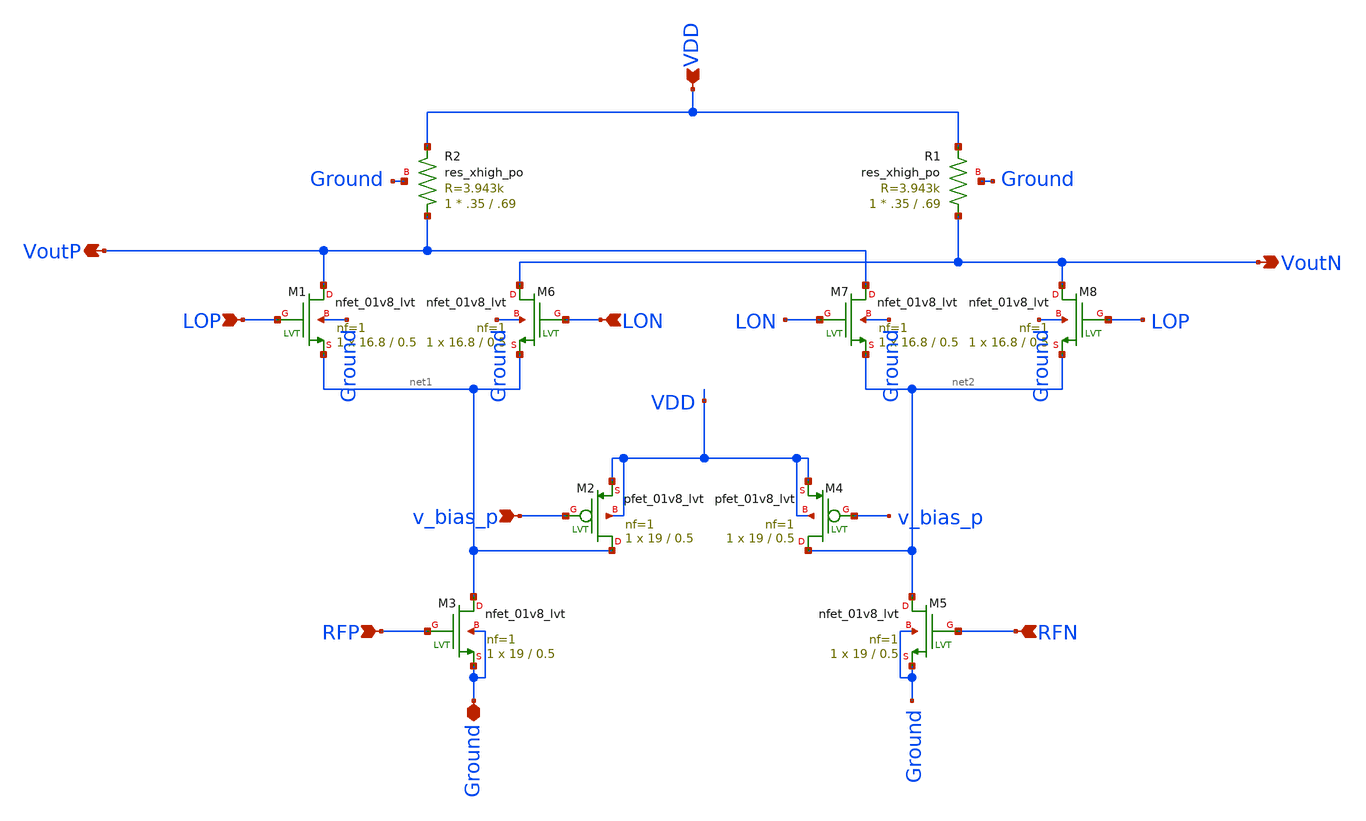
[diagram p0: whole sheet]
** sch_path: skywater_stuff/ECE631_RF_CMOS/Mixer_LVS_test1.sch
**.subckt Mixer_LVS_test1 v_bias_p RFP RFN LOP LON VoutP VoutN Ground VDD
*.ipin v_bias_p
*.ipin RFP
*.ipin RFN
*.ipin LOP
*.ipin LON
*.opin VoutP
*.opin VoutN
*.iopin Ground
*.ipin VDD
XM1 VoutP LOP net1 Ground sky130_fd_pr__nfet_01v8_lvt L=0.5 W=16.8 nf=1 ad='int((nf+1)/2) * W/nf * 0.29'
+ as='int((nf+2)/2) * W/nf * 0.29' pd='2*int((nf+1)/2) * (W/nf + 0.29)' ps='2*int((nf+2)/2) * (W/nf + 0.29)'
+ nrd='0.29 / W' nrs='0.29 / W' sa=0 sb=0 sd=0 mult=1 m=1
XM2 net1 v_bias_p VDD VDD sky130_fd_pr__pfet_01v8_lvt L=0.5 W=19 nf=1 ad='int((nf+1)/2) * W/nf * 0.29'
+ as='int((nf+2)/2) * W/nf * 0.29' pd='2*int((nf+1)/2) * (W/nf + 0.29)' ps='2*int((nf+2)/2) * (W/nf + 0.29)'
+ nrd='0.29 / W' nrs='0.29 / W' sa=0 sb=0 sd=0 mult=1 m=1
XM6 VoutN LON net1 Ground sky130_fd_pr__nfet_01v8_lvt L=0.5 W=16.8 nf=1 ad='int((nf+1)/2) * W/nf * 0.29'
+ as='int((nf+2)/2) * W/nf * 0.29' pd='2*int((nf+1)/2) * (W/nf + 0.29)' ps='2*int((nf+2)/2) * (W/nf + 0.29)'
+ nrd='0.29 / W' nrs='0.29 / W' sa=0 sb=0 sd=0 mult=1 m=1
XM7 VoutP LON net2 Ground sky130_fd_pr__nfet_01v8_lvt L=0.5 W=16.8 nf=1 ad='int((nf+1)/2) * W/nf * 0.29'
+ as='int((nf+2)/2) * W/nf * 0.29' pd='2*int((nf+1)/2) * (W/nf + 0.29)' ps='2*int((nf+2)/2) * (W/nf + 0.29)'
+ nrd='0.29 / W' nrs='0.29 / W' sa=0 sb=0 sd=0 mult=1 m=1
XM8 VoutN LOP net2 Ground sky130_fd_pr__nfet_01v8_lvt L=0.5 W=16.8 nf=1 ad='int((nf+1)/2) * W/nf * 0.29'
+ as='int((nf+2)/2) * W/nf * 0.29' pd='2*int((nf+1)/2) * (W/nf + 0.29)' ps='2*int((nf+2)/2) * (W/nf + 0.29)'
+ nrd='0.29 / W' nrs='0.29 / W' sa=0 sb=0 sd=0 mult=1 m=1
XM3 net1 RFP Ground Ground sky130_fd_pr__nfet_01v8_lvt L=0.5 W=19 nf=1 ad='int((nf+1)/2) * W/nf * 0.29'
+ as='int((nf+2)/2) * W/nf * 0.29' pd='2*int((nf+1)/2) * (W/nf + 0.29)' ps='2*int((nf+2)/2) * (W/nf + 0.29)'
+ nrd='0.29 / W' nrs='0.29 / W' sa=0 sb=0 sd=0 mult=1 m=1
XM4 net2 v_bias_p VDD VDD sky130_fd_pr__pfet_01v8_lvt L=0.5 W=19 nf=1 ad='int((nf+1)/2) * W/nf * 0.29'
+ as='int((nf+2)/2) * W/nf * 0.29' pd='2*int((nf+1)/2) * (W/nf + 0.29)' ps='2*int((nf+2)/2) * (W/nf + 0.29)'
+ nrd='0.29 / W' nrs='0.29 / W' sa=0 sb=0 sd=0 mult=1 m=1
XM5 net2 RFN Ground Ground sky130_fd_pr__nfet_01v8_lvt L=0.5 W=19 nf=1 ad='int((nf+1)/2) * W/nf * 0.29'
+ as='int((nf+2)/2) * W/nf * 0.29' pd='2*int((nf+1)/2) * (W/nf + 0.29)' ps='2*int((nf+2)/2) * (W/nf + 0.29)'
+ nrd='0.29 / W' nrs='0.29 / W' sa=0 sb=0 sd=0 mult=1 m=1
XR2 VoutP VDD Ground sky130_fd_pr__res_xhigh_po W=.35 L=.69 mult=1 m=1
XR1 VoutN VDD Ground sky130_fd_pr__res_xhigh_po W=.35 L=.69 mult=1 m=1
**.ends
.end
